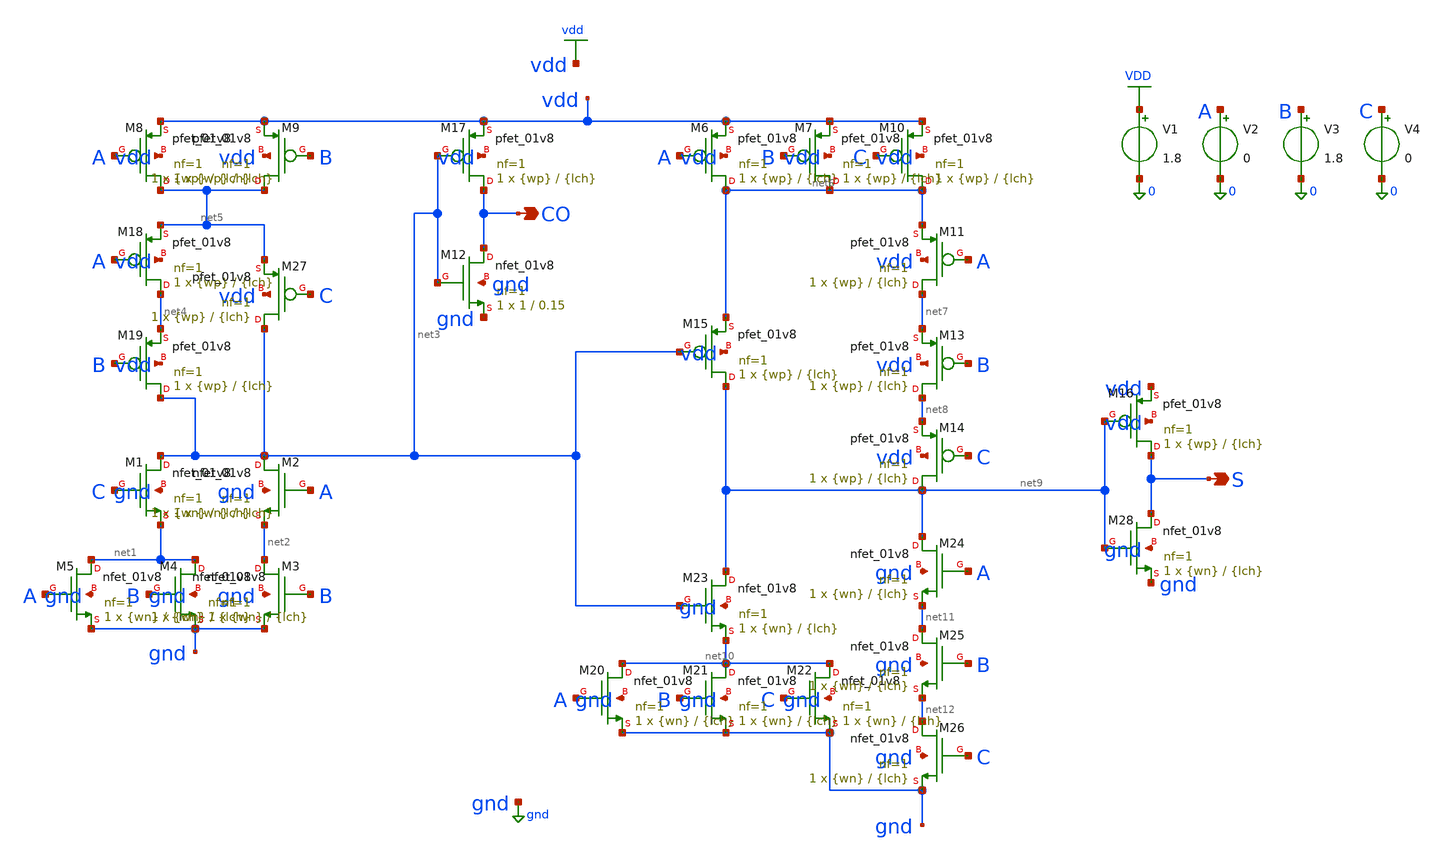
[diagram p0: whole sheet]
** sch_path: tb_WLfulladder.sch
**.subckt tb_WLfulladder CO S
*.opin CO
*.opin S
XM2 net3 A net2 gnd sky130_fd_pr__nfet_01v8 L={lch} W={wn} nf=1 ad='int((1 + 1)/2) * {wn} / 1 * 0.29'
+ as='int((1 + 2)/2) * {wn} / 1 * 0.29' pd='2*int((1 + 1)/2) * ({wn} / 1 + 0.29)' ps='2*int((1 + 2)/2) * ({wn} / 1 + 0.29)'
+ nrd='0.29 / {wn} ' nrs='0.29 / {wn} ' sa=0 sb=0 sd=0 mult=1 m=1
XM8 net5 A vdd vdd sky130_fd_pr__pfet_01v8 L={lch} W={wp} nf=1 ad='int((1 + 1)/2) * {wp} / 1 * 0.29'
+ as='int((1 + 2)/2) * {wp} / 1 * 0.29' pd='2*int((1 + 1)/2) * ({wp} / 1 + 0.29)' ps='2*int((1 + 2)/2) * ({wp} / 1 + 0.29)'
+ nrd='0.29 / {wp} ' nrs='0.29 / {wp} ' sa=0 sb=0 sd=0 mult=1 m=1
XM12 CO net3 gnd gnd sky130_fd_pr__nfet_01v8 L=0.15 W=1 nf=1 ad='int((1 + 1)/2) * 1 / 1 * 0.29' as='int((1 + 2)/2) * 1 / 1 * 0.29'
+ pd='2*int((1 + 1)/2) * (1 / 1 + 0.29)' ps='2*int((1 + 2)/2) * (1 / 1 + 0.29)' nrd='0.29 / 1 ' nrs='0.29 / 1 '
+ sa=0 sb=0 sd=0 mult=1 m=1
V1 VDD 0 1.8
V2 A 0 0
V3 B 0 1.8
V4 C 0 0
XM9 net5 B vdd vdd sky130_fd_pr__pfet_01v8 L={lch} W={wp} nf=1 ad='int((1 + 1)/2) * {wp} / 1 * 0.29'
+ as='int((1 + 2)/2) * {wp} / 1 * 0.29' pd='2*int((1 + 1)/2) * ({wp} / 1 + 0.29)' ps='2*int((1 + 2)/2) * ({wp} / 1 + 0.29)'
+ nrd='0.29 / {wp} ' nrs='0.29 / {wp} ' sa=0 sb=0 sd=0 mult=1 m=1
XM6 net6 A vdd vdd sky130_fd_pr__pfet_01v8 L={lch} W={wp} nf=1 ad='int((1 + 1)/2) * {wp} / 1 * 0.29'
+ as='int((1 + 2)/2) * {wp} / 1 * 0.29' pd='2*int((1 + 1)/2) * ({wp} / 1 + 0.29)' ps='2*int((1 + 2)/2) * ({wp} / 1 + 0.29)'
+ nrd='0.29 / {wp} ' nrs='0.29 / {wp} ' sa=0 sb=0 sd=0 mult=1 m=1
XM7 net6 B vdd vdd sky130_fd_pr__pfet_01v8 L={lch} W={wp} nf=1 ad='int((1 + 1)/2) * {wp} / 1 * 0.29'
+ as='int((1 + 2)/2) * {wp} / 1 * 0.29' pd='2*int((1 + 1)/2) * ({wp} / 1 + 0.29)' ps='2*int((1 + 2)/2) * ({wp} / 1 + 0.29)'
+ nrd='0.29 / {wp} ' nrs='0.29 / {wp} ' sa=0 sb=0 sd=0 mult=1 m=1
XM10 net6 C vdd vdd sky130_fd_pr__pfet_01v8 L={lch} W={wp} nf=1 ad='int((1 + 1)/2) * {wp} / 1 * 0.29'
+ as='int((1 + 2)/2) * {wp} / 1 * 0.29' pd='2*int((1 + 1)/2) * ({wp} / 1 + 0.29)' ps='2*int((1 + 2)/2) * ({wp} / 1 + 0.29)'
+ nrd='0.29 / {wp} ' nrs='0.29 / {wp} ' sa=0 sb=0 sd=0 mult=1 m=1
XM11 net7 A net6 vdd sky130_fd_pr__pfet_01v8 L={lch} W={wp} nf=1 ad='int((1 + 1)/2) * {wp} / 1 * 0.29'
+ as='int((1 + 2)/2) * {wp} / 1 * 0.29' pd='2*int((1 + 1)/2) * ({wp} / 1 + 0.29)' ps='2*int((1 + 2)/2) * ({wp} / 1 + 0.29)'
+ nrd='0.29 / {wp} ' nrs='0.29 / {wp} ' sa=0 sb=0 sd=0 mult=1 m=1
XM13 net8 B net7 vdd sky130_fd_pr__pfet_01v8 L={lch} W={wp} nf=1 ad='int((1 + 1)/2) * {wp} / 1 * 0.29'
+ as='int((1 + 2)/2) * {wp} / 1 * 0.29' pd='2*int((1 + 1)/2) * ({wp} / 1 + 0.29)' ps='2*int((1 + 2)/2) * ({wp} / 1 + 0.29)'
+ nrd='0.29 / {wp} ' nrs='0.29 / {wp} ' sa=0 sb=0 sd=0 mult=1 m=1
XM14 net9 C net8 vdd sky130_fd_pr__pfet_01v8 L={lch} W={wp} nf=1 ad='int((1 + 1)/2) * {wp} / 1 * 0.29'
+ as='int((1 + 2)/2) * {wp} / 1 * 0.29' pd='2*int((1 + 1)/2) * ({wp} / 1 + 0.29)' ps='2*int((1 + 2)/2) * ({wp} / 1 + 0.29)'
+ nrd='0.29 / {wp} ' nrs='0.29 / {wp} ' sa=0 sb=0 sd=0 mult=1 m=1
XM15 net9 net3 net6 vdd sky130_fd_pr__pfet_01v8 L={lch} W={wp} nf=1 ad='int((1 + 1)/2) * {wp} / 1 * 0.29'
+ as='int((1 + 2)/2) * {wp} / 1 * 0.29' pd='2*int((1 + 1)/2) * ({wp} / 1 + 0.29)' ps='2*int((1 + 2)/2) * ({wp} / 1 + 0.29)'
+ nrd='0.29 / {wp} ' nrs='0.29 / {wp} ' sa=0 sb=0 sd=0 mult=1 m=1
XM16 S net9 vdd vdd sky130_fd_pr__pfet_01v8 L={lch} W={wp} nf=1 ad='int((1 + 1)/2) * {wp} / 1 * 0.29'
+ as='int((1 + 2)/2) * {wp} / 1 * 0.29' pd='2*int((1 + 1)/2) * ({wp} / 1 + 0.29)' ps='2*int((1 + 2)/2) * ({wp} / 1 + 0.29)'
+ nrd='0.29 / {wp} ' nrs='0.29 / {wp} ' sa=0 sb=0 sd=0 mult=1 m=1
XM17 CO net3 vdd vdd sky130_fd_pr__pfet_01v8 L={lch} W={wp} nf=1 ad='int((1 + 1)/2) * {wp} / 1 * 0.29'
+ as='int((1 + 2)/2) * {wp} / 1 * 0.29' pd='2*int((1 + 1)/2) * ({wp} / 1 + 0.29)' ps='2*int((1 + 2)/2) * ({wp} / 1 + 0.29)'
+ nrd='0.29 / {wp} ' nrs='0.29 / {wp} ' sa=0 sb=0 sd=0 mult=1 m=1
XM18 net4 A net5 vdd sky130_fd_pr__pfet_01v8 L={lch} W={wp} nf=1 ad='int((1 + 1)/2) * {wp} / 1 * 0.29'
+ as='int((1 + 2)/2) * {wp} / 1 * 0.29' pd='2*int((1 + 1)/2) * ({wp} / 1 + 0.29)' ps='2*int((1 + 2)/2) * ({wp} / 1 + 0.29)'
+ nrd='0.29 / {wp} ' nrs='0.29 / {wp} ' sa=0 sb=0 sd=0 mult=1 m=1
XM19 net3 B net4 vdd sky130_fd_pr__pfet_01v8 L={lch} W={wp} nf=1 ad='int((1 + 1)/2) * {wp} / 1 * 0.29'
+ as='int((1 + 2)/2) * {wp} / 1 * 0.29' pd='2*int((1 + 1)/2) * ({wp} / 1 + 0.29)' ps='2*int((1 + 2)/2) * ({wp} / 1 + 0.29)'
+ nrd='0.29 / {wp} ' nrs='0.29 / {wp} ' sa=0 sb=0 sd=0 mult=1 m=1
XM27 net3 C net5 vdd sky130_fd_pr__pfet_01v8 L={lch} W={wp} nf=1 ad='int((1 + 1)/2) * {wp} / 1 * 0.29'
+ as='int((1 + 2)/2) * {wp} / 1 * 0.29' pd='2*int((1 + 1)/2) * ({wp} / 1 + 0.29)' ps='2*int((1 + 2)/2) * ({wp} / 1 + 0.29)'
+ nrd='0.29 / {wp} ' nrs='0.29 / {wp} ' sa=0 sb=0 sd=0 mult=1 m=1
XM1 net3 C net1 gnd sky130_fd_pr__nfet_01v8 L={lch} W={wn} nf=1 ad='int((1 + 1)/2) * {wn} / 1 * 0.29'
+ as='int((1 + 2)/2) * {wn} / 1 * 0.29' pd='2*int((1 + 1)/2) * ({wn} / 1 + 0.29)' ps='2*int((1 + 2)/2) * ({wn} / 1 + 0.29)'
+ nrd='0.29 / {wn} ' nrs='0.29 / {wn} ' sa=0 sb=0 sd=0 mult=1 m=1
XM3 net2 B gnd gnd sky130_fd_pr__nfet_01v8 L={lch} W={wn} nf=1 ad='int((1 + 1)/2) * {wn} / 1 * 0.29'
+ as='int((1 + 2)/2) * {wn} / 1 * 0.29' pd='2*int((1 + 1)/2) * ({wn} / 1 + 0.29)' ps='2*int((1 + 2)/2) * ({wn} / 1 + 0.29)'
+ nrd='0.29 / {wn} ' nrs='0.29 / {wn} ' sa=0 sb=0 sd=0 mult=1 m=1
XM4 net1 B gnd gnd sky130_fd_pr__nfet_01v8 L={lch} W={wn} nf=1 ad='int((1 + 1)/2) * {wn} / 1 * 0.29'
+ as='int((1 + 2)/2) * {wn} / 1 * 0.29' pd='2*int((1 + 1)/2) * ({wn} / 1 + 0.29)' ps='2*int((1 + 2)/2) * ({wn} / 1 + 0.29)'
+ nrd='0.29 / {wn} ' nrs='0.29 / {wn} ' sa=0 sb=0 sd=0 mult=1 m=1
XM5 net1 A gnd gnd sky130_fd_pr__nfet_01v8 L={lch} W={wn} nf=1 ad='int((1 + 1)/2) * {wn} / 1 * 0.29'
+ as='int((1 + 2)/2) * {wn} / 1 * 0.29' pd='2*int((1 + 1)/2) * ({wn} / 1 + 0.29)' ps='2*int((1 + 2)/2) * ({wn} / 1 + 0.29)'
+ nrd='0.29 / {wn} ' nrs='0.29 / {wn} ' sa=0 sb=0 sd=0 mult=1 m=1
XM20 net10 A gnd gnd sky130_fd_pr__nfet_01v8 L={lch} W={wn} nf=1 ad='int((1 + 1)/2) * {wn} / 1 * 0.29'
+ as='int((1 + 2)/2) * {wn} / 1 * 0.29' pd='2*int((1 + 1)/2) * ({wn} / 1 + 0.29)' ps='2*int((1 + 2)/2) * ({wn} / 1 + 0.29)'
+ nrd='0.29 / {wn} ' nrs='0.29 / {wn} ' sa=0 sb=0 sd=0 mult=1 m=1
XM21 net10 B gnd gnd sky130_fd_pr__nfet_01v8 L={lch} W={wn} nf=1 ad='int((1 + 1)/2) * {wn} / 1 * 0.29'
+ as='int((1 + 2)/2) * {wn} / 1 * 0.29' pd='2*int((1 + 1)/2) * ({wn} / 1 + 0.29)' ps='2*int((1 + 2)/2) * ({wn} / 1 + 0.29)'
+ nrd='0.29 / {wn} ' nrs='0.29 / {wn} ' sa=0 sb=0 sd=0 mult=1 m=1
XM22 net10 C gnd gnd sky130_fd_pr__nfet_01v8 L={lch} W={wn} nf=1 ad='int((1 + 1)/2) * {wn} / 1 * 0.29'
+ as='int((1 + 2)/2) * {wn} / 1 * 0.29' pd='2*int((1 + 1)/2) * ({wn} / 1 + 0.29)' ps='2*int((1 + 2)/2) * ({wn} / 1 + 0.29)'
+ nrd='0.29 / {wn} ' nrs='0.29 / {wn} ' sa=0 sb=0 sd=0 mult=1 m=1
XM23 net9 net3 net10 gnd sky130_fd_pr__nfet_01v8 L={lch} W={wn} nf=1 ad='int((1 + 1)/2) * {wn} / 1 * 0.29'
+ as='int((1 + 2)/2) * {wn} / 1 * 0.29' pd='2*int((1 + 1)/2) * ({wn} / 1 + 0.29)' ps='2*int((1 + 2)/2) * ({wn} / 1 + 0.29)'
+ nrd='0.29 / {wn} ' nrs='0.29 / {wn} ' sa=0 sb=0 sd=0 mult=1 m=1
XM24 net9 A net11 gnd sky130_fd_pr__nfet_01v8 L={lch} W={wn} nf=1 ad='int((1 + 1)/2) * {wn} / 1 * 0.29'
+ as='int((1 + 2)/2) * {wn} / 1 * 0.29' pd='2*int((1 + 1)/2) * ({wn} / 1 + 0.29)' ps='2*int((1 + 2)/2) * ({wn} / 1 + 0.29)'
+ nrd='0.29 / {wn} ' nrs='0.29 / {wn} ' sa=0 sb=0 sd=0 mult=1 m=1
XM25 net11 B net12 gnd sky130_fd_pr__nfet_01v8 L={lch} W={wn} nf=1 ad='int((1 + 1)/2) * {wn} / 1 * 0.29'
+ as='int((1 + 2)/2) * {wn} / 1 * 0.29' pd='2*int((1 + 1)/2) * ({wn} / 1 + 0.29)' ps='2*int((1 + 2)/2) * ({wn} / 1 + 0.29)'
+ nrd='0.29 / {wn} ' nrs='0.29 / {wn} ' sa=0 sb=0 sd=0 mult=1 m=1
XM26 net12 C gnd gnd sky130_fd_pr__nfet_01v8 L={lch} W={wn} nf=1 ad='int((1 + 1)/2) * {wn} / 1 * 0.29'
+ as='int((1 + 2)/2) * {wn} / 1 * 0.29' pd='2*int((1 + 1)/2) * ({wn} / 1 + 0.29)' ps='2*int((1 + 2)/2) * ({wn} / 1 + 0.29)'
+ nrd='0.29 / {wn} ' nrs='0.29 / {wn} ' sa=0 sb=0 sd=0 mult=1 m=1
XM28 S net9 gnd gnd sky130_fd_pr__nfet_01v8 L={lch} W={wn} nf=1 ad='int((1 + 1)/2) * {wn} / 1 * 0.29'
+ as='int((1 + 2)/2) * {wn} / 1 * 0.29' pd='2*int((1 + 1)/2) * ({wn} / 1 + 0.29)' ps='2*int((1 + 2)/2) * ({wn} / 1 + 0.29)'
+ nrd='0.29 / {wn} ' nrs='0.29 / {wn} ' sa=0 sb=0 sd=0 mult=1 m=1
**** begin user architecture code
.lib /foss/pdks/sky130A/libs.tech/ngspice/sky130.lib.spice tt
.param wp=2 wn=1 lch=0.15
.control
foreach w 1 1.5 2 2.5 3 3.5 4 4.5 5
    alterparam wp = $w
    reset
    dc V2 0 1.8 0.02
    meas dc vm_sum WHEN v(s)=0.9
    meas dc vm_cout WHEN v(co)=0.9

    echo $w $&vm_sum $&vm_cout >> /foss/designs/dc_results.txt
    write /foss/designs/dc_wp{$w}.raw v(a) v(s) v(co)
end
.endc
.end

**** end user architecture code
**.ends
.GLOBAL vdd
.GLOBAL gnd
.GLOBAL VDD
.end
